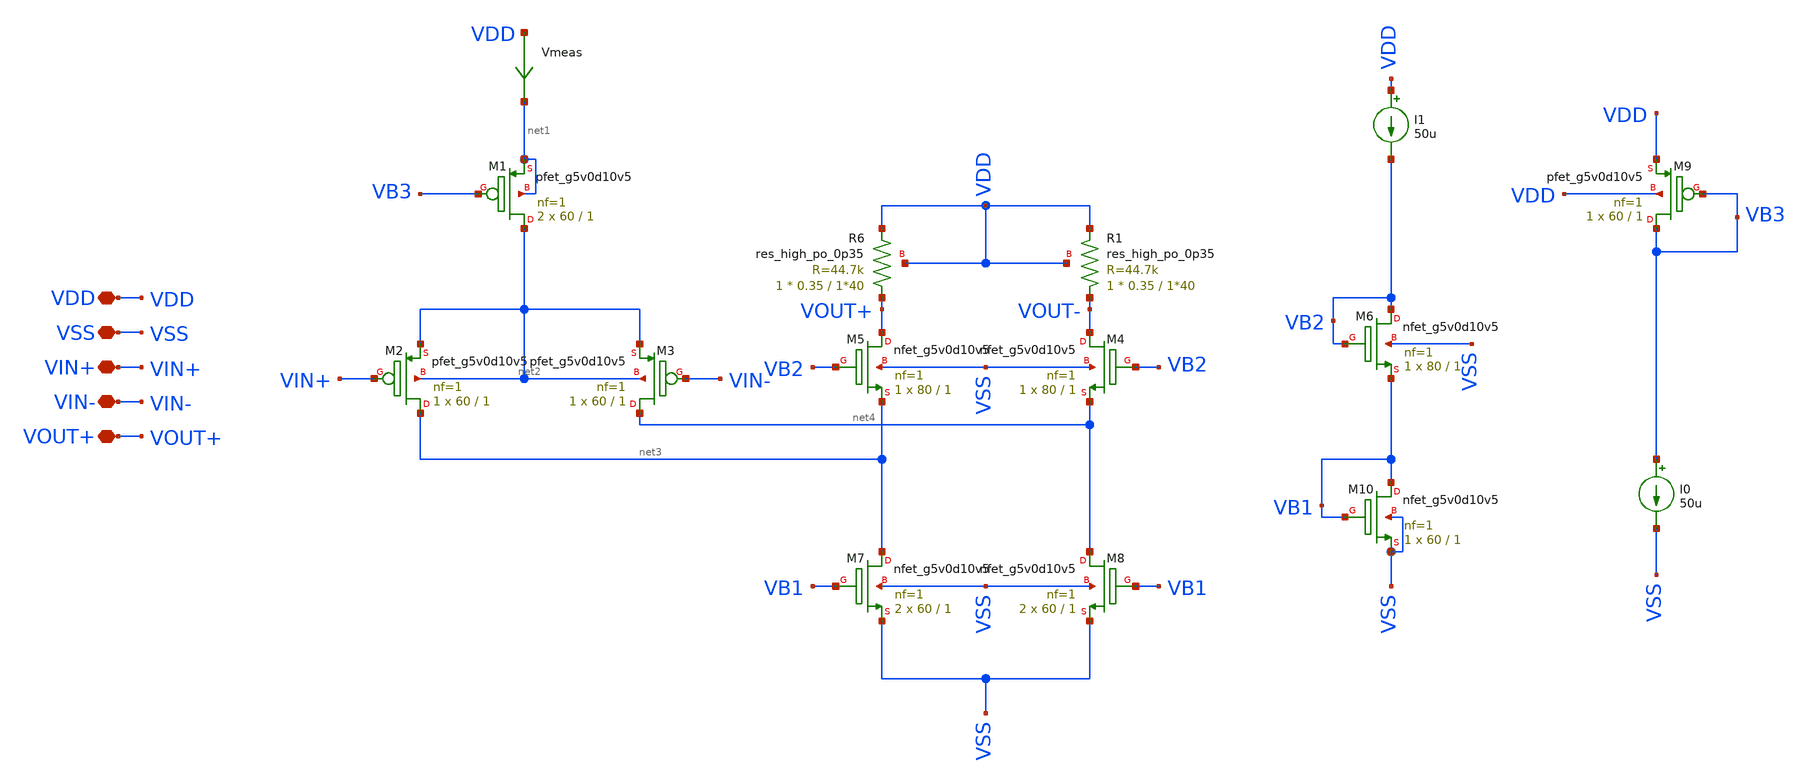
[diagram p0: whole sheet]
** sch_path: old stuff/amplifiers/differencial_stage_amps/stange stages/folded_cascode/differential_stage.sch
**.subckt differential_stage VDD VSS VIN+ VIN- VOUT+
*.iopin VDD
*.iopin VSS
*.iopin VIN+
*.iopin VIN-
*.iopin VOUT+
I0 VB3 VSS 50u
Vmeas VDD net1 0
.save i(vmeas)
XM9 VB3 VB3 VDD VDD sky130_fd_pr__pfet_g5v0d10v5 L=1 W=60 nf=1 ad='int((1 + 1)/2) * 60 / 1 * 0.29' as='int((1 + 2)/2) * 60 / 1 * 0.29'
+ pd='2*int((1 + 1)/2) * (60 / 1 + 0.29)' ps='2*int((1 + 2)/2) * (60 / 1 + 0.29)' nrd='0.29 / 60 ' nrs='0.29 / 60 '
+ sa=0 sb=0 sd=0 mult=1 m=1
XM1 net2 VB3 net1 net1 sky130_fd_pr__pfet_g5v0d10v5 L=1 W=60 nf=1 ad='int((1 + 1)/2) * 60 / 1 * 0.29'
+ as='int((1 + 2)/2) * 60 / 1 * 0.29' pd='2*int((1 + 1)/2) * (60 / 1 + 0.29)' ps='2*int((1 + 2)/2) * (60 / 1 + 0.29)'
+ nrd='0.29 / 60 ' nrs='0.29 / 60 ' sa=0 sb=0 sd=0 mult=2 m=2
XM2 net3 VIN+ net2 net2 sky130_fd_pr__pfet_g5v0d10v5 L=1 W=60 nf=1 ad='int((1 + 1)/2) * 60 / 1 * 0.29'
+ as='int((1 + 2)/2) * 60 / 1 * 0.29' pd='2*int((1 + 1)/2) * (60 / 1 + 0.29)' ps='2*int((1 + 2)/2) * (60 / 1 + 0.29)'
+ nrd='0.29 / 60 ' nrs='0.29 / 60 ' sa=0 sb=0 sd=0 mult=1 m=1
XM3 net4 VIN- net2 net2 sky130_fd_pr__pfet_g5v0d10v5 L=1 W=60 nf=1 ad='int((1 + 1)/2) * 60 / 1 * 0.29'
+ as='int((1 + 2)/2) * 60 / 1 * 0.29' pd='2*int((1 + 1)/2) * (60 / 1 + 0.29)' ps='2*int((1 + 2)/2) * (60 / 1 + 0.29)'
+ nrd='0.29 / 60 ' nrs='0.29 / 60 ' sa=0 sb=0 sd=0 mult=1 m=1
XR6 VOUT+ VDD VDD sky130_fd_pr__res_high_po_0p35 L=1*40 mult=1 m=1
XR1 VOUT- VDD VDD sky130_fd_pr__res_high_po_0p35 L=1*40 mult=1 m=1
XM5 VOUT+ VB2 net3 VSS sky130_fd_pr__nfet_g5v0d10v5 L=1 W=80 nf=1 ad='int((1 + 1)/2) * 80 / 1 * 0.29'
+ as='int((1 + 2)/2) * 80 / 1 * 0.29' pd='2*int((1 + 1)/2) * (80 / 1 + 0.29)' ps='2*int((1 + 2)/2) * (80 / 1 + 0.29)'
+ nrd='0.29 / 80 ' nrs='0.29 / 80 ' sa=0 sb=0 sd=0 mult=1 m=1
XM4 VOUT- VB2 net4 VSS sky130_fd_pr__nfet_g5v0d10v5 L=1 W=80 nf=1 ad='int((1 + 1)/2) * 80 / 1 * 0.29'
+ as='int((1 + 2)/2) * 80 / 1 * 0.29' pd='2*int((1 + 1)/2) * (80 / 1 + 0.29)' ps='2*int((1 + 2)/2) * (80 / 1 + 0.29)'
+ nrd='0.29 / 80 ' nrs='0.29 / 80 ' sa=0 sb=0 sd=0 mult=1 m=1
I1 VDD VB2 50u
XM6 VB2 VB2 VB1 VSS sky130_fd_pr__nfet_g5v0d10v5 L=1 W=80 nf=1 ad='int((1 + 1)/2) * 80 / 1 * 0.29' as='int((1 + 2)/2) * 80 / 1 * 0.29'
+ pd='2*int((1 + 1)/2) * (80 / 1 + 0.29)' ps='2*int((1 + 2)/2) * (80 / 1 + 0.29)' nrd='0.29 / 80 ' nrs='0.29 / 80 '
+ sa=0 sb=0 sd=0 mult=1 m=1
XM7 net3 VB1 VSS VSS sky130_fd_pr__nfet_g5v0d10v5 L=1 W=60 nf=1 ad='int((1 + 1)/2) * 60 / 1 * 0.29' as='int((1 + 2)/2) * 60 / 1 * 0.29'
+ pd='2*int((1 + 1)/2) * (60 / 1 + 0.29)' ps='2*int((1 + 2)/2) * (60 / 1 + 0.29)' nrd='0.29 / 60 ' nrs='0.29 / 60 '
+ sa=0 sb=0 sd=0 mult=2 m=2
XM8 net4 VB1 VSS VSS sky130_fd_pr__nfet_g5v0d10v5 L=1 W=60 nf=1 ad='int((1 + 1)/2) * 60 / 1 * 0.29' as='int((1 + 2)/2) * 60 / 1 * 0.29'
+ pd='2*int((1 + 1)/2) * (60 / 1 + 0.29)' ps='2*int((1 + 2)/2) * (60 / 1 + 0.29)' nrd='0.29 / 60 ' nrs='0.29 / 60 '
+ sa=0 sb=0 sd=0 mult=2 m=2
XM10 VB1 VB1 VSS VSS sky130_fd_pr__nfet_g5v0d10v5 L=1 W=60 nf=1 ad='int((1 + 1)/2) * 60 / 1 * 0.29' as='int((1 + 2)/2) * 60 / 1 * 0.29'
+ pd='2*int((1 + 1)/2) * (60 / 1 + 0.29)' ps='2*int((1 + 2)/2) * (60 / 1 + 0.29)' nrd='0.29 / 60 ' nrs='0.29 / 60 '
+ sa=0 sb=0 sd=0 mult=1 m=1
**.ends
.end
